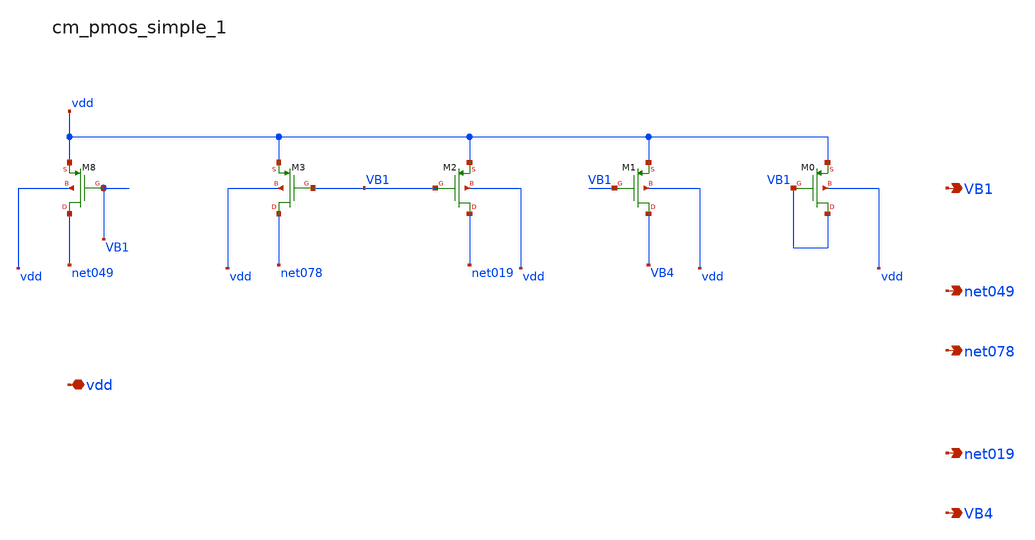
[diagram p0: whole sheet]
** sch_path: analog-db/raw/amp_013_qu2017_azc/hier/blocks/cm_pmos_simple_1.sch
**.subckt cm_pmos_simple_1 vdd VB1 net049 net078 net019 VB4
*.iopin vdd
*.opin VB1
*.opin net049
*.opin net078
*.opin net019
*.opin VB4
XM0 VB1 VB1 vdd vdd sg13_lv_pmos w=x_dut_xm0_w l=x_dut_xm0_l ng=1 m=x_dut_xm0_m
XM1 VB4 VB1 vdd vdd sg13_lv_pmos w=x_dut_xm1_w l=x_dut_xm1_l ng=1 m=x_dut_xm1_m
XM2 net019 VB1 vdd vdd sg13_lv_pmos w=x_dut_xm2_w l=x_dut_xm2_l ng=1 m=x_dut_xm2_m
XM3 net078 VB1 vdd vdd sg13_lv_pmos w=x_dut_xm3_w l=x_dut_xm3_l ng=1 m=x_dut_xm3_m
XM8 net049 VB1 vdd vdd sg13_lv_pmos w=x_dut_xm8_w l=x_dut_xm8_l ng=1 m=x_dut_xm8_m
**.ends
.end
